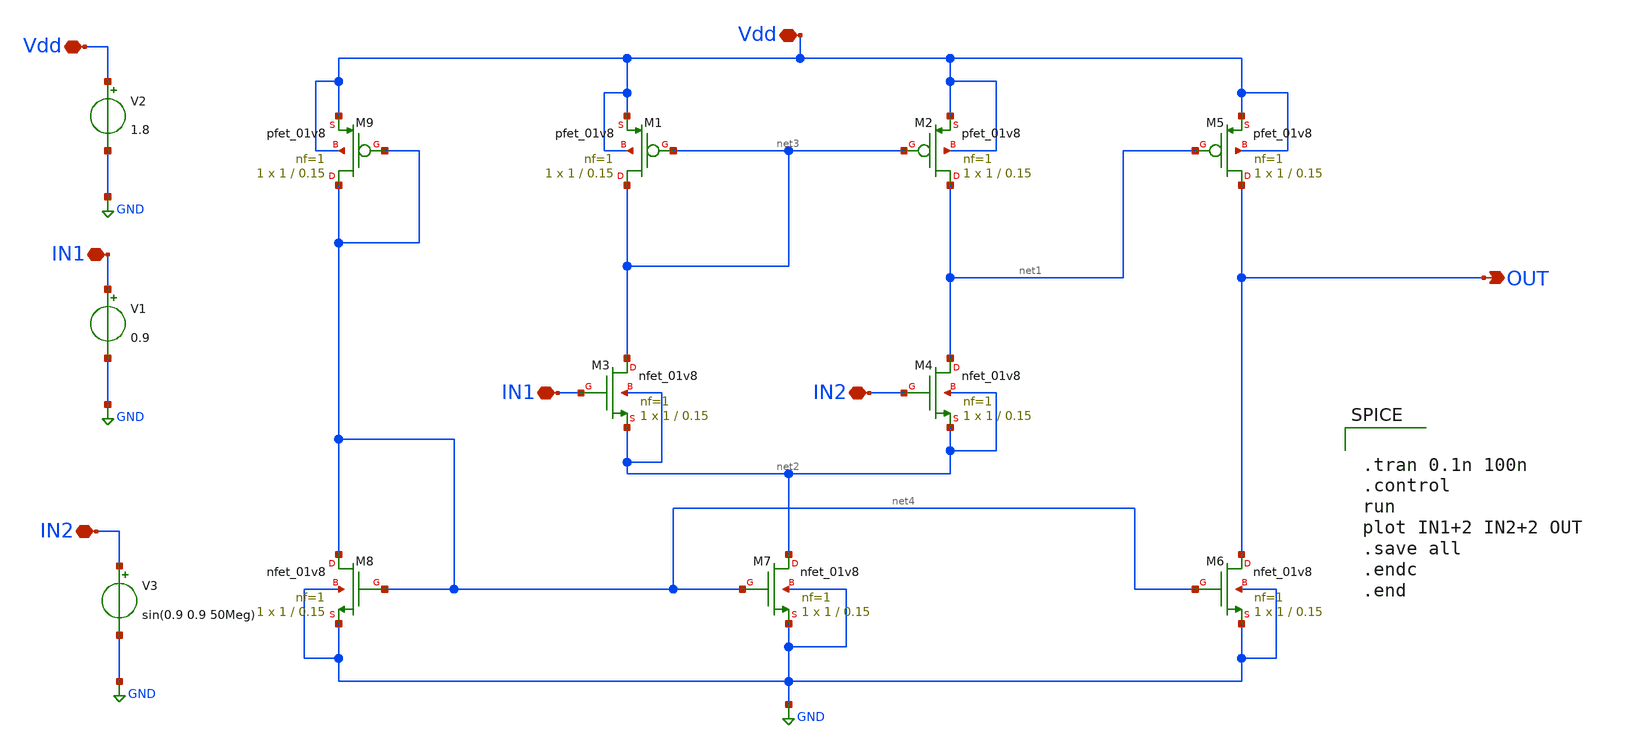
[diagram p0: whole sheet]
** sch_path: Week_4/OneBitADC_PreLayout/1_bit_ADC_pre.sch
**.subckt 1_bit_ADC_pre OUT Vdd IN1 IN2 IN2 IN1 Vdd
*.opin OUT
*.iopin Vdd
*.iopin IN1
*.iopin IN2
*.iopin IN2
*.iopin IN1
*.iopin Vdd
XM2 net1 net3 Vdd Vdd sky130_fd_pr__pfet_01v8 L=0.15 W=1 nf=1 ad='int((nf+1)/2) * W/nf * 0.29' as='int((nf+2)/2) * W/nf * 0.29'
+ pd='2*int((nf+1)/2) * (W/nf + 0.29)' ps='2*int((nf+2)/2) * (W/nf + 0.29)' nrd='0.29 / W' nrs='0.29 / W'
+ sa=0 sb=0 sd=0 mult=1 m=1
XM3 net3 IN1 net2 net2 sky130_fd_pr__nfet_01v8 L=0.15 W=1 nf=1 ad='int((nf+1)/2) * W/nf * 0.29' as='int((nf+2)/2) * W/nf * 0.29'
+ pd='2*int((nf+1)/2) * (W/nf + 0.29)' ps='2*int((nf+2)/2) * (W/nf + 0.29)' nrd='0.29 / W' nrs='0.29 / W'
+ sa=0 sb=0 sd=0 mult=1 m=1
XM4 net1 IN2 net2 net2 sky130_fd_pr__nfet_01v8 L=0.15 W=1 nf=1 ad='int((nf+1)/2) * W/nf * 0.29' as='int((nf+2)/2) * W/nf * 0.29'
+ pd='2*int((nf+1)/2) * (W/nf + 0.29)' ps='2*int((nf+2)/2) * (W/nf + 0.29)' nrd='0.29 / W' nrs='0.29 / W'
+ sa=0 sb=0 sd=0 mult=1 m=1
XM1 net3 net3 Vdd Vdd sky130_fd_pr__pfet_01v8 L=0.15 W=1 nf=1 ad='int((nf+1)/2) * W/nf * 0.29' as='int((nf+2)/2) * W/nf * 0.29'
+ pd='2*int((nf+1)/2) * (W/nf + 0.29)' ps='2*int((nf+2)/2) * (W/nf + 0.29)' nrd='0.29 / W' nrs='0.29 / W'
+ sa=0 sb=0 sd=0 mult=1 m=1
XM5 OUT net1 Vdd Vdd sky130_fd_pr__pfet_01v8 L=0.15 W=1 nf=1 ad='int((nf+1)/2) * W/nf * 0.29' as='int((nf+2)/2) * W/nf * 0.29'
+ pd='2*int((nf+1)/2) * (W/nf + 0.29)' ps='2*int((nf+2)/2) * (W/nf + 0.29)' nrd='0.29 / W' nrs='0.29 / W'
+ sa=0 sb=0 sd=0 mult=1 m=1
XM6 OUT net4 GND GND sky130_fd_pr__nfet_01v8 L=0.15 W=1 nf=1 ad='int((nf+1)/2) * W/nf * 0.29' as='int((nf+2)/2) * W/nf * 0.29'
+ pd='2*int((nf+1)/2) * (W/nf + 0.29)' ps='2*int((nf+2)/2) * (W/nf + 0.29)' nrd='0.29 / W' nrs='0.29 / W'
+ sa=0 sb=0 sd=0 mult=1 m=1
XM7 net2 net4 GND GND sky130_fd_pr__nfet_01v8 L=0.15 W=1 nf=1 ad='int((nf+1)/2) * W/nf * 0.29' as='int((nf+2)/2) * W/nf * 0.29'
+ pd='2*int((nf+1)/2) * (W/nf + 0.29)' ps='2*int((nf+2)/2) * (W/nf + 0.29)' nrd='0.29 / W' nrs='0.29 / W'
+ sa=0 sb=0 sd=0 mult=1 m=1
XM8 net4 net4 GND GND sky130_fd_pr__nfet_01v8 L=0.15 W=1 nf=1 ad='int((nf+1)/2) * W/nf * 0.29' as='int((nf+2)/2) * W/nf * 0.29'
+ pd='2*int((nf+1)/2) * (W/nf + 0.29)' ps='2*int((nf+2)/2) * (W/nf + 0.29)' nrd='0.29 / W' nrs='0.29 / W'
+ sa=0 sb=0 sd=0 mult=1 m=1
XM9 net4 net4 Vdd Vdd sky130_fd_pr__pfet_01v8 L=0.15 W=1 nf=1 ad='int((nf+1)/2) * W/nf * 0.29' as='int((nf+2)/2) * W/nf * 0.29'
+ pd='2*int((nf+1)/2) * (W/nf + 0.29)' ps='2*int((nf+2)/2) * (W/nf + 0.29)' nrd='0.29 / W' nrs='0.29 / W'
+ sa=0 sb=0 sd=0 mult=1 m=1
V3 IN2 GND sin(0.9 0.9 50Meg)
V1 IN1 GND 0.9
V2 Vdd GND 1.8
**** begin user architecture code


.tran 0.1n 100n
.control
run
plot IN1+2 IN2+2 OUT
.save all
.endc
.end




.lib /home/swagatika/open_pdks/sky130/sky130A/libs.tech/ngspice/sky130.lib.spice tt

.save all



**** end user architecture code
**.ends
.GLOBAL GND
.end
